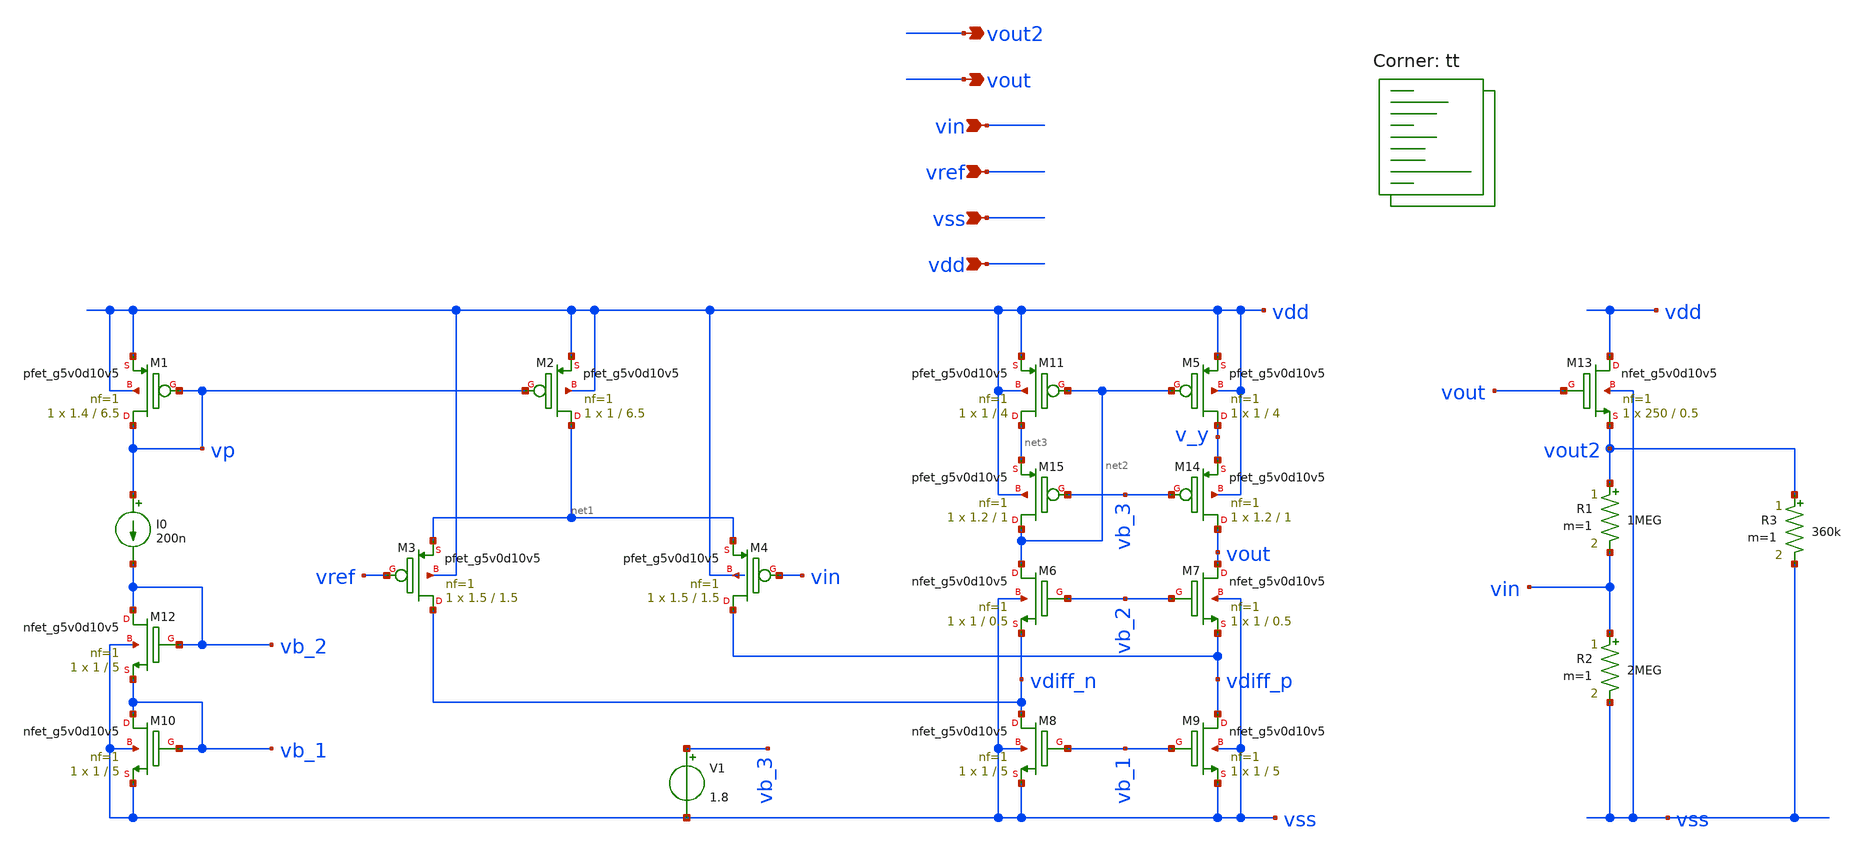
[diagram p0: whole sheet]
** sch_path: xschem/error_amp.sch
**.subckt error_amp vout vin vref vss vdd vout2
*.opin vout
*.ipin vin
*.ipin vref
*.ipin vss
*.ipin vdd
*.opin vout2
I0 vp vb_2 200n
XM1 vp vp vdd vdd sky130_fd_pr__pfet_g5v0d10v5 L=6.5 W=1.4 nf=1 ad='int((nf+1)/2) * W/nf * 0.29' as='int((nf+2)/2) * W/nf * 0.29'
+ pd='2*int((nf+1)/2) * (W/nf + 0.29)' ps='2*int((nf+2)/2) * (W/nf + 0.29)' nrd='0.29 / W' nrs='0.29 / W'
+ sa=0 sb=0 sd=0 mult=1 m=1
XM2 net1 vp vdd vdd sky130_fd_pr__pfet_g5v0d10v5 L=6.5 W=1 nf=1 ad='int((nf+1)/2) * W/nf * 0.29' as='int((nf+2)/2) * W/nf * 0.29'
+ pd='2*int((nf+1)/2) * (W/nf + 0.29)' ps='2*int((nf+2)/2) * (W/nf + 0.29)' nrd='0.29 / W' nrs='0.29 / W'
+ sa=0 sb=0 sd=0 mult=1 m=1
XM3 vdiff_n vref net1 vdd sky130_fd_pr__pfet_g5v0d10v5 L=1.5 W=1.5 nf=1 ad='int((nf+1)/2) * W/nf * 0.29'
+ as='int((nf+2)/2) * W/nf * 0.29' pd='2*int((nf+1)/2) * (W/nf + 0.29)' ps='2*int((nf+2)/2) * (W/nf + 0.29)'
+ nrd='0.29 / W' nrs='0.29 / W' sa=0 sb=0 sd=0 mult=1 m=1
XM4 vdiff_p vin net1 vdd sky130_fd_pr__pfet_g5v0d10v5 L=1.5 W=1.5 nf=1 ad='int((nf+1)/2) * W/nf * 0.29'
+ as='int((nf+2)/2) * W/nf * 0.29' pd='2*int((nf+1)/2) * (W/nf + 0.29)' ps='2*int((nf+2)/2) * (W/nf + 0.29)'
+ nrd='0.29 / W' nrs='0.29 / W' sa=0 sb=0 sd=0 mult=1 m=1
XM5 v_y net2 vdd vdd sky130_fd_pr__pfet_g5v0d10v5 L=4 W=1 nf=1 ad='int((nf+1)/2) * W/nf * 0.29' as='int((nf+2)/2) * W/nf * 0.29'
+ pd='2*int((nf+1)/2) * (W/nf + 0.29)' ps='2*int((nf+2)/2) * (W/nf + 0.29)' nrd='0.29 / W' nrs='0.29 / W'
+ sa=0 sb=0 sd=0 mult=1 m=1
XM6 net2 vb_2 vdiff_n vss sky130_fd_pr__nfet_g5v0d10v5 L=0.5 W=1 nf=1 ad='int((nf+1)/2) * W/nf * 0.29'
+ as='int((nf+2)/2) * W/nf * 0.29' pd='2*int((nf+1)/2) * (W/nf + 0.29)' ps='2*int((nf+2)/2) * (W/nf + 0.29)'
+ nrd='0.29 / W' nrs='0.29 / W' sa=0 sb=0 sd=0 mult=1 m=1
XM7 vout vb_2 vdiff_p vss sky130_fd_pr__nfet_g5v0d10v5 L=0.5 W=1 nf=1 ad='int((nf+1)/2) * W/nf * 0.29'
+ as='int((nf+2)/2) * W/nf * 0.29' pd='2*int((nf+1)/2) * (W/nf + 0.29)' ps='2*int((nf+2)/2) * (W/nf + 0.29)'
+ nrd='0.29 / W' nrs='0.29 / W' sa=0 sb=0 sd=0 mult=1 m=1
XM8 vdiff_n vb_1 vss vss sky130_fd_pr__nfet_g5v0d10v5 L=5 W=1 nf=1 ad='int((nf+1)/2) * W/nf * 0.29' as='int((nf+2)/2) * W/nf * 0.29'
+ pd='2*int((nf+1)/2) * (W/nf + 0.29)' ps='2*int((nf+2)/2) * (W/nf + 0.29)' nrd='0.29 / W' nrs='0.29 / W'
+ sa=0 sb=0 sd=0 mult=1 m=1
XM9 vdiff_p vb_1 vss vss sky130_fd_pr__nfet_g5v0d10v5 L=5 W=1 nf=1 ad='int((nf+1)/2) * W/nf * 0.29' as='int((nf+2)/2) * W/nf * 0.29'
+ pd='2*int((nf+1)/2) * (W/nf + 0.29)' ps='2*int((nf+2)/2) * (W/nf + 0.29)' nrd='0.29 / W' nrs='0.29 / W'
+ sa=0 sb=0 sd=0 mult=1 m=1
XM10 vb_1 vb_1 vss vss sky130_fd_pr__nfet_g5v0d10v5 L=5 W=1 nf=1 ad='int((nf+1)/2) * W/nf * 0.29' as='int((nf+2)/2) * W/nf * 0.29'
+ pd='2*int((nf+1)/2) * (W/nf + 0.29)' ps='2*int((nf+2)/2) * (W/nf + 0.29)' nrd='0.29 / W' nrs='0.29 / W'
+ sa=0 sb=0 sd=0 mult=1 m=1
XM11 net3 net2 vdd vdd sky130_fd_pr__pfet_g5v0d10v5 L=4 W=1 nf=1 ad='int((nf+1)/2) * W/nf * 0.29' as='int((nf+2)/2) * W/nf * 0.29'
+ pd='2*int((nf+1)/2) * (W/nf + 0.29)' ps='2*int((nf+2)/2) * (W/nf + 0.29)' nrd='0.29 / W' nrs='0.29 / W'
+ sa=0 sb=0 sd=0 mult=1 m=1
XM12 vb_2 vb_2 vb_1 vss sky130_fd_pr__nfet_g5v0d10v5 L=5 W=1 nf=1 ad='int((nf+1)/2) * W/nf * 0.29' as='int((nf+2)/2) * W/nf * 0.29'
+ pd='2*int((nf+1)/2) * (W/nf + 0.29)' ps='2*int((nf+2)/2) * (W/nf + 0.29)' nrd='0.29 / W' nrs='0.29 / W'
+ sa=0 sb=0 sd=0 mult=1 m=1
XM13 vdd vout vout2 vss sky130_fd_pr__nfet_g5v0d10v5 L=0.5 W=250 nf=1 ad='int((nf+1)/2) * W/nf * 0.29'
+ as='int((nf+2)/2) * W/nf * 0.29' pd='2*int((nf+1)/2) * (W/nf + 0.29)' ps='2*int((nf+2)/2) * (W/nf + 0.29)'
+ nrd='0.29 / W' nrs='0.29 / W' sa=0 sb=0 sd=0 mult=1 m=1
R1 vout2 vin 1MEG m=1
R2 vin vss 2MEG m=1
R3 vout2 vss 360k m=1
XM14 vout vb_3 v_y vdd sky130_fd_pr__pfet_g5v0d10v5 L=1 W=1.2 nf=1 ad='int((nf+1)/2) * W/nf * 0.29' as='int((nf+2)/2) * W/nf * 0.29'
+ pd='2*int((nf+1)/2) * (W/nf + 0.29)' ps='2*int((nf+2)/2) * (W/nf + 0.29)' nrd='0.29 / W' nrs='0.29 / W'
+ sa=0 sb=0 sd=0 mult=1 m=1
XM15 net2 vb_3 net3 vdd sky130_fd_pr__pfet_g5v0d10v5 L=1 W=1.2 nf=1 ad='int((nf+1)/2) * W/nf * 0.29'
+ as='int((nf+2)/2) * W/nf * 0.29' pd='2*int((nf+1)/2) * (W/nf + 0.29)' ps='2*int((nf+2)/2) * (W/nf + 0.29)'
+ nrd='0.29 / W' nrs='0.29 / W' sa=0 sb=0 sd=0 mult=1 m=1
V1 vb_3 vss 1.8
**** begin user architecture code

vdd vdd 0 3.3 ac 1
* vdd1 vdd1 0 3.3
vss vss 0 0
vref vref 0 1.2
* vin vin 0 1.2 ac 1
.option savecurrents
.control
save all
save @m.xm13.msky130_fd_pr__nfet_g5v0d10v5[cgs]
save @m.xm5.msky130_fd_pr__pfet_g5v0d10v5[gds]
op
print @m.xm13.msky130_fd_pr__nfet_g5v0d10v5[cgs]
print @m.xm5.msky130_fd_pr__pfet_g5v0d10v5[gds]
write error_amp.raw
set appendwrite
ac dec 10 10 1e9
write error_amp.raw
set units=degrees
plot db(vout) db(vout2)
plot ph(vout) ph(vout2)
.endc


.lib $::SKYWATER_MODELS/sky130.lib.spice tt
**** end user architecture code
**.ends
.end
